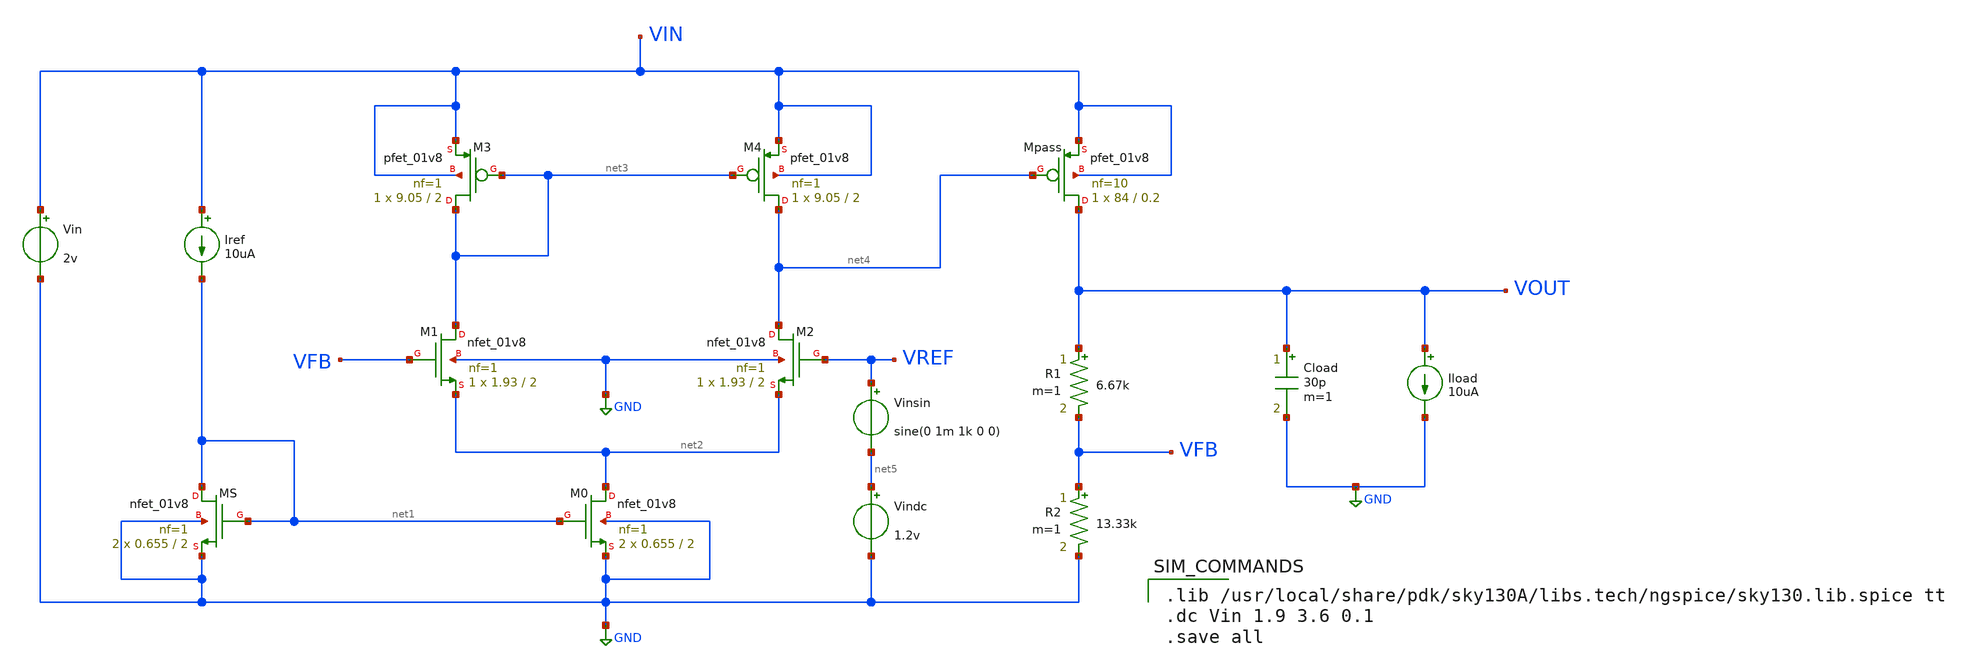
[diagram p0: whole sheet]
** sch_path: Simulation/dcSweepSimMinLoadMaxCap.sch
**.subckt dcSweepSimMinLoadMaxCap
XMS net1 net1 GND GND sky130_fd_pr__nfet_01v8 L=2 W=0.655 nf=1 ad='int((nf+1)/2) * W/nf * 0.29' as='int((nf+2)/2) * W/nf * 0.29'
+ pd='2*int((nf+1)/2) * (W/nf + 0.29)' ps='2*int((nf+2)/2) * (W/nf + 0.29)' nrd='0.29 / W' nrs='0.29 / W'
+ sa=0 sb=0 sd=0 mult=2 m=2
XM0 net2 net1 GND GND sky130_fd_pr__nfet_01v8 L=2 W=0.655 nf=1 ad='int((nf+1)/2) * W/nf * 0.29' as='int((nf+2)/2) * W/nf * 0.29'
+ pd='2*int((nf+1)/2) * (W/nf + 0.29)' ps='2*int((nf+2)/2) * (W/nf + 0.29)' nrd='0.29 / W' nrs='0.29 / W'
+ sa=0 sb=0 sd=0 mult=2 m=2
XM1 net3 VFB net2 GND sky130_fd_pr__nfet_01v8 L=2 W=1.93 nf=1 ad='int((nf+1)/2) * W/nf * 0.29' as='int((nf+2)/2) * W/nf * 0.29'
+ pd='2*int((nf+1)/2) * (W/nf + 0.29)' ps='2*int((nf+2)/2) * (W/nf + 0.29)' nrd='0.29 / W' nrs='0.29 / W'
+ sa=0 sb=0 sd=0 mult=1 m=1
XM2 net4 VREF net2 GND sky130_fd_pr__nfet_01v8 L=2 W=1.93 nf=1 ad='int((nf+1)/2) * W/nf * 0.29' as='int((nf+2)/2) * W/nf * 0.29'
+ pd='2*int((nf+1)/2) * (W/nf + 0.29)' ps='2*int((nf+2)/2) * (W/nf + 0.29)' nrd='0.29 / W' nrs='0.29 / W'
+ sa=0 sb=0 sd=0 mult=1 m=1
XM4 net4 net3 VIN VIN sky130_fd_pr__pfet_01v8 L=2 W=9.05 nf=1 ad='int((nf+1)/2) * W/nf * 0.29' as='int((nf+2)/2) * W/nf * 0.29'
+ pd='2*int((nf+1)/2) * (W/nf + 0.29)' ps='2*int((nf+2)/2) * (W/nf + 0.29)' nrd='0.29 / W' nrs='0.29 / W'
+ sa=0 sb=0 sd=0 mult=1 m=1
XM3 net3 net3 VIN VIN sky130_fd_pr__pfet_01v8 L=2 W=9.05 nf=1 ad='int((nf+1)/2) * W/nf * 0.29' as='int((nf+2)/2) * W/nf * 0.29'
+ pd='2*int((nf+1)/2) * (W/nf + 0.29)' ps='2*int((nf+2)/2) * (W/nf + 0.29)' nrd='0.29 / W' nrs='0.29 / W'
+ sa=0 sb=0 sd=0 mult=1 m=1
Vin VIN GND 2v
Iref VIN net1 10uA
Vindc net5 GND 1.2v
XMpass VOUT net4 VIN VIN sky130_fd_pr__pfet_01v8 L=0.2 W=84 nf=10 ad='int((nf+1)/2) * W/nf * 0.29' as='int((nf+2)/2) * W/nf * 0.29'
+ pd='2*int((nf+1)/2) * (W/nf + 0.29)' ps='2*int((nf+2)/2) * (W/nf + 0.29)' nrd='0.29 / W' nrs='0.29 / W'
+ sa=0 sb=0 sd=0 mult=1 m=1
R1 VOUT VFB 6.67k m=1
R2 VFB GND 13.33k m=1
Vinsin VREF net5 sine(0 1m 1k 0 0)
Cload VOUT GND 30p m=1
Iload VOUT GND 10uA
**** begin user architecture code

.lib /usr/local/share/pdk/sky130A/libs.tech/ngspice/sky130.lib.spice tt
.dc Vin 1.9 3.6 0.1
.save all

**** end user architecture code
**.ends
.GLOBAL GND
.end
